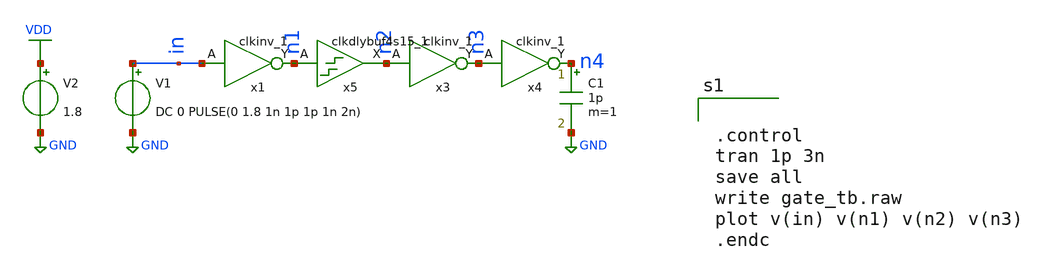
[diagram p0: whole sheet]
** sch_path: verification/analog_modulator/gate_tb.sch
**.subckt gate_tb
V1 in GND DC 0 PULSE(0 1.8 1n 1p 1p 1n 2n)
C1 n4 GND 1p m=1
V2 VDD GND 1.8
x1 in GND GND VDD VDD n1 sky130_fd_sc_hd__clkinv_1
x3 n2 GND GND VDD VDD n3 sky130_fd_sc_hd__clkinv_1
x4 n3 GND GND VDD VDD n4 sky130_fd_sc_hd__clkinv_1
x5 n1 GND GND VDD VDD n2 sky130_fd_sc_hd__clkdlybuf4s15_1
**** begin user architecture code

** opencircuitdesign pdks install
.lib /farmshare/home/classes/ee/372/PDKs/open_pdks_1.0.310/sky130/sky130A/libs.tech/ngspice/sky130.lib.spice tt
.inc /farmshare/home/classes/ee/372/PDKs/open_pdks_1.0.310/sky130/sky130A/libs.ref/sky130_fd_sc_hd/spice/sky130_fd_sc_hd.spice



.control
tran 1p 3n
save all
write gate_tb.raw
plot v(in) v(n1) v(n2) v(n3)
.endc


**** end user architecture code
**.ends
.GLOBAL GND
.GLOBAL VDD
.end
